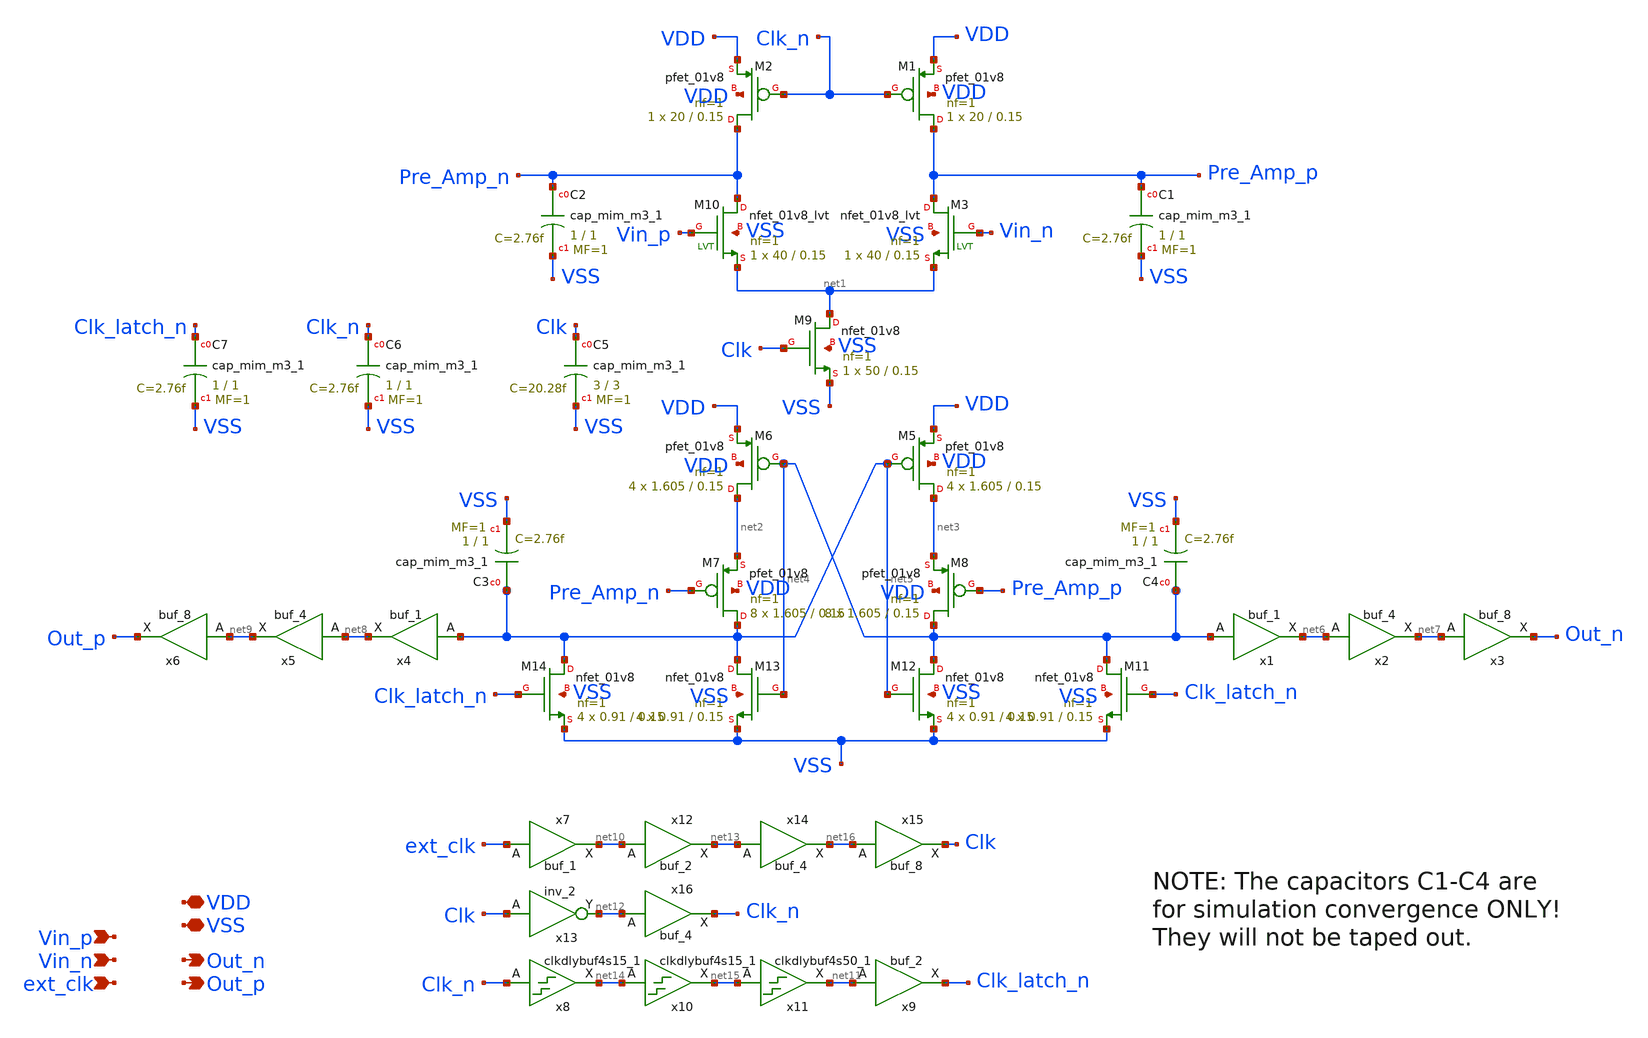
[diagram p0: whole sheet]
** sch_path: xschem/src/comparator/comparator_low_vt.sch
**.subckt comparator_low_vt VDD VSS Vin_p Out_n Vin_n Out_p ext_clk
*.iopin VDD
*.iopin VSS
*.ipin Vin_p
*.opin Out_n
*.ipin Vin_n
*.opin Out_p
*.ipin ext_clk
XM1 Pre_Amp_p Clk_n VDD VDD sky130_fd_pr__pfet_01v8 L=0.15 W=20 nf=1 ad='int((nf+1)/2) * W/nf * 0.29'
+ as='int((nf+2)/2) * W/nf * 0.29' pd='2*int((nf+1)/2) * (W/nf + 0.29)' ps='2*int((nf+2)/2) * (W/nf + 0.29)'
+ nrd='0.29 / W' nrs='0.29 / W' sa=0 sb=0 sd=0 mult=1 m=1
XM2 Pre_Amp_n Clk_n VDD VDD sky130_fd_pr__pfet_01v8 L=0.15 W=20 nf=1 ad='int((nf+1)/2) * W/nf * 0.29'
+ as='int((nf+2)/2) * W/nf * 0.29' pd='2*int((nf+1)/2) * (W/nf + 0.29)' ps='2*int((nf+2)/2) * (W/nf + 0.29)'
+ nrd='0.29 / W' nrs='0.29 / W' sa=0 sb=0 sd=0 mult=1 m=1
XM5 net3 net5 VDD VDD sky130_fd_pr__pfet_01v8 L=0.15 W=1.605 nf=1 ad='int((nf+1)/2) * W/nf * 0.29' as='int((nf+2)/2) * W/nf * 0.29'
+ pd='2*int((nf+1)/2) * (W/nf + 0.29)' ps='2*int((nf+2)/2) * (W/nf + 0.29)' nrd='0.29 / W' nrs='0.29 / W'
+ sa=0 sb=0 sd=0 mult=4 m=4
XM6 net2 net4 VDD VDD sky130_fd_pr__pfet_01v8 L=0.15 W=1.605 nf=1 ad='int((nf+1)/2) * W/nf * 0.29' as='int((nf+2)/2) * W/nf * 0.29'
+ pd='2*int((nf+1)/2) * (W/nf + 0.29)' ps='2*int((nf+2)/2) * (W/nf + 0.29)' nrd='0.29 / W' nrs='0.29 / W'
+ sa=0 sb=0 sd=0 mult=4 m=4
XM9 net1 Clk VSS VSS sky130_fd_pr__nfet_01v8 L=0.15 W=50 nf=1 ad='int((nf+1)/2) * W/nf * 0.29' as='int((nf+2)/2) * W/nf * 0.29'
+ pd='2*int((nf+1)/2) * (W/nf + 0.29)' ps='2*int((nf+2)/2) * (W/nf + 0.29)' nrd='0.29 / W' nrs='0.29 / W'
+ sa=0 sb=0 sd=0 mult=1 m=1
XM11 net4 Clk_latch_n VSS VSS sky130_fd_pr__nfet_01v8 L=0.15 W=0.91 nf=1 ad='int((nf+1)/2) * W/nf * 0.29'
+ as='int((nf+2)/2) * W/nf * 0.29' pd='2*int((nf+1)/2) * (W/nf + 0.29)' ps='2*int((nf+2)/2) * (W/nf + 0.29)'
+ nrd='0.29 / W' nrs='0.29 / W' sa=0 sb=0 sd=0 mult=4 m=4
XM12 net4 net5 VSS VSS sky130_fd_pr__nfet_01v8 L=0.15 W=0.91 nf=1 ad='int((nf+1)/2) * W/nf * 0.29' as='int((nf+2)/2) * W/nf * 0.29'
+ pd='2*int((nf+1)/2) * (W/nf + 0.29)' ps='2*int((nf+2)/2) * (W/nf + 0.29)' nrd='0.29 / W' nrs='0.29 / W'
+ sa=0 sb=0 sd=0 mult=4 m=4
XM13 net5 net4 VSS VSS sky130_fd_pr__nfet_01v8 L=0.15 W=0.91 nf=1 ad='int((nf+1)/2) * W/nf * 0.29' as='int((nf+2)/2) * W/nf * 0.29'
+ pd='2*int((nf+1)/2) * (W/nf + 0.29)' ps='2*int((nf+2)/2) * (W/nf + 0.29)' nrd='0.29 / W' nrs='0.29 / W'
+ sa=0 sb=0 sd=0 mult=4 m=4
XM14 net5 Clk_latch_n VSS VSS sky130_fd_pr__nfet_01v8 L=0.15 W=0.91 nf=1 ad='int((nf+1)/2) * W/nf * 0.29'
+ as='int((nf+2)/2) * W/nf * 0.29' pd='2*int((nf+1)/2) * (W/nf + 0.29)' ps='2*int((nf+2)/2) * (W/nf + 0.29)'
+ nrd='0.29 / W' nrs='0.29 / W' sa=0 sb=0 sd=0 mult=4 m=4
XM7 net5 Pre_Amp_n net2 VDD sky130_fd_pr__pfet_01v8 L=0.15 W=1.605 nf=1 ad='int((nf+1)/2) * W/nf * 0.29'
+ as='int((nf+2)/2) * W/nf * 0.29' pd='2*int((nf+1)/2) * (W/nf + 0.29)' ps='2*int((nf+2)/2) * (W/nf + 0.29)'
+ nrd='0.29 / W' nrs='0.29 / W' sa=0 sb=0 sd=0 mult=8 m=8
XM8 net4 Pre_Amp_p net3 VDD sky130_fd_pr__pfet_01v8 L=0.15 W=1.605 nf=1 ad='int((nf+1)/2) * W/nf * 0.29'
+ as='int((nf+2)/2) * W/nf * 0.29' pd='2*int((nf+1)/2) * (W/nf + 0.29)' ps='2*int((nf+2)/2) * (W/nf + 0.29)'
+ nrd='0.29 / W' nrs='0.29 / W' sa=0 sb=0 sd=0 mult=8 m=8
XC1 Pre_Amp_p VSS sky130_fd_pr__cap_mim_m3_1 W=1 L=1 MF=1 m=1
XC2 Pre_Amp_n VSS sky130_fd_pr__cap_mim_m3_1 W=1 L=1 MF=1 m=1
x1 net4 VSS VSS VDD VDD net6 sky130_fd_sc_hd__buf_1
x2 net6 VSS VSS VDD VDD net7 sky130_fd_sc_hd__buf_4
x3 net7 VSS VSS VDD VDD Out_n sky130_fd_sc_hd__buf_8
x4 net5 VSS VSS VDD VDD net8 sky130_fd_sc_hd__buf_1
x5 net8 VSS VSS VDD VDD net9 sky130_fd_sc_hd__buf_4
x6 net9 VSS VSS VDD VDD Out_p sky130_fd_sc_hd__buf_8
XC3 net5 VSS sky130_fd_pr__cap_mim_m3_1 W=1 L=1 MF=1 m=1
XC4 net4 VSS sky130_fd_pr__cap_mim_m3_1 W=1 L=1 MF=1 m=1
x7 ext_clk VSS VSS VDD VDD net10 sky130_fd_sc_hd__buf_1
x8 Clk_n VSS VSS VDD VDD net14 sky130_fd_sc_hd__clkdlybuf4s15_1
x9 net11 VSS VSS VDD VDD Clk_latch_n sky130_fd_sc_hd__buf_2
x10 net14 VSS VSS VDD VDD net15 sky130_fd_sc_hd__clkdlybuf4s15_1
x11 net15 VSS VSS VDD VDD net11 sky130_fd_sc_hd__clkdlybuf4s50_1
x13 Clk VSS VSS VDD VDD net12 sky130_fd_sc_hd__inv_2
x12 net10 VSS VSS VDD VDD net13 sky130_fd_sc_hd__buf_2
x14 net13 VSS VSS VDD VDD net16 sky130_fd_sc_hd__buf_4
x15 net16 VSS VSS VDD VDD Clk sky130_fd_sc_hd__buf_8
XC5 Clk VSS sky130_fd_pr__cap_mim_m3_1 W=3 L=3 MF=1 m=1
XC6 Clk_n VSS sky130_fd_pr__cap_mim_m3_1 W=1 L=1 MF=1 m=1
XC7 Clk_latch_n VSS sky130_fd_pr__cap_mim_m3_1 W=1 L=1 MF=1 m=1
x16 net12 VSS VSS VDD VDD Clk_n sky130_fd_sc_hd__buf_4
XM10 Pre_Amp_n Vin_p net1 VSS sky130_fd_pr__nfet_01v8_lvt L=0.15 W=40 nf=1 ad='int((nf+1)/2) * W/nf * 0.29'
+ as='int((nf+2)/2) * W/nf * 0.29' pd='2*int((nf+1)/2) * (W/nf + 0.29)' ps='2*int((nf+2)/2) * (W/nf + 0.29)'
+ nrd='0.29 / W' nrs='0.29 / W' sa=0 sb=0 sd=0 mult=1 m=1
XM3 Pre_Amp_p Vin_n net1 VSS sky130_fd_pr__nfet_01v8_lvt L=0.15 W=40 nf=1 ad='int((nf+1)/2) * W/nf * 0.29'
+ as='int((nf+2)/2) * W/nf * 0.29' pd='2*int((nf+1)/2) * (W/nf + 0.29)' ps='2*int((nf+2)/2) * (W/nf + 0.29)'
+ nrd='0.29 / W' nrs='0.29 / W' sa=0 sb=0 sd=0 mult=1 m=1
**.ends
.end
